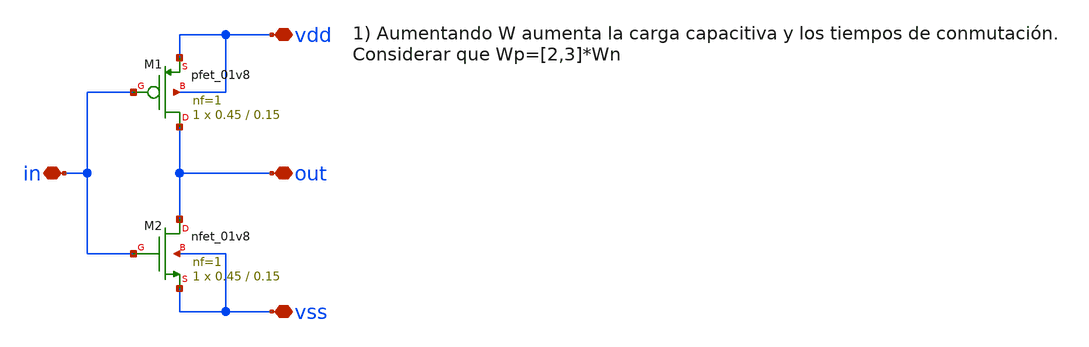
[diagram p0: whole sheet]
** sch_path: designs/sch/inverter.sch
**.subckt inverter out vss vdd in
*.iopin out
*.iopin vss
*.iopin vdd
*.iopin in
XM2 out in vss vss sky130_fd_pr__nfet_01v8 L=0.15 W=0.45 nf=1 ad='int((nf+1)/2) * W/nf * 0.29' as='int((nf+2)/2) * W/nf * 0.29'
+ pd='2*int((nf+1)/2) * (W/nf + 0.29)' ps='2*int((nf+2)/2) * (W/nf + 0.29)' nrd='0.29 / W' nrs='0.29 / W'
+ sa=0 sb=0 sd=0 mult=1 m=1
XM1 out in vdd vdd sky130_fd_pr__pfet_01v8 L=0.15 W=0.45 nf=1 ad='int((nf+1)/2) * W/nf * 0.29' as='int((nf+2)/2) * W/nf * 0.29'
+ pd='2*int((nf+1)/2) * (W/nf + 0.29)' ps='2*int((nf+2)/2) * (W/nf + 0.29)' nrd='0.29 / W' nrs='0.29 / W'
+ sa=0 sb=0 sd=0 mult=1 m=1
**.ends
.end
